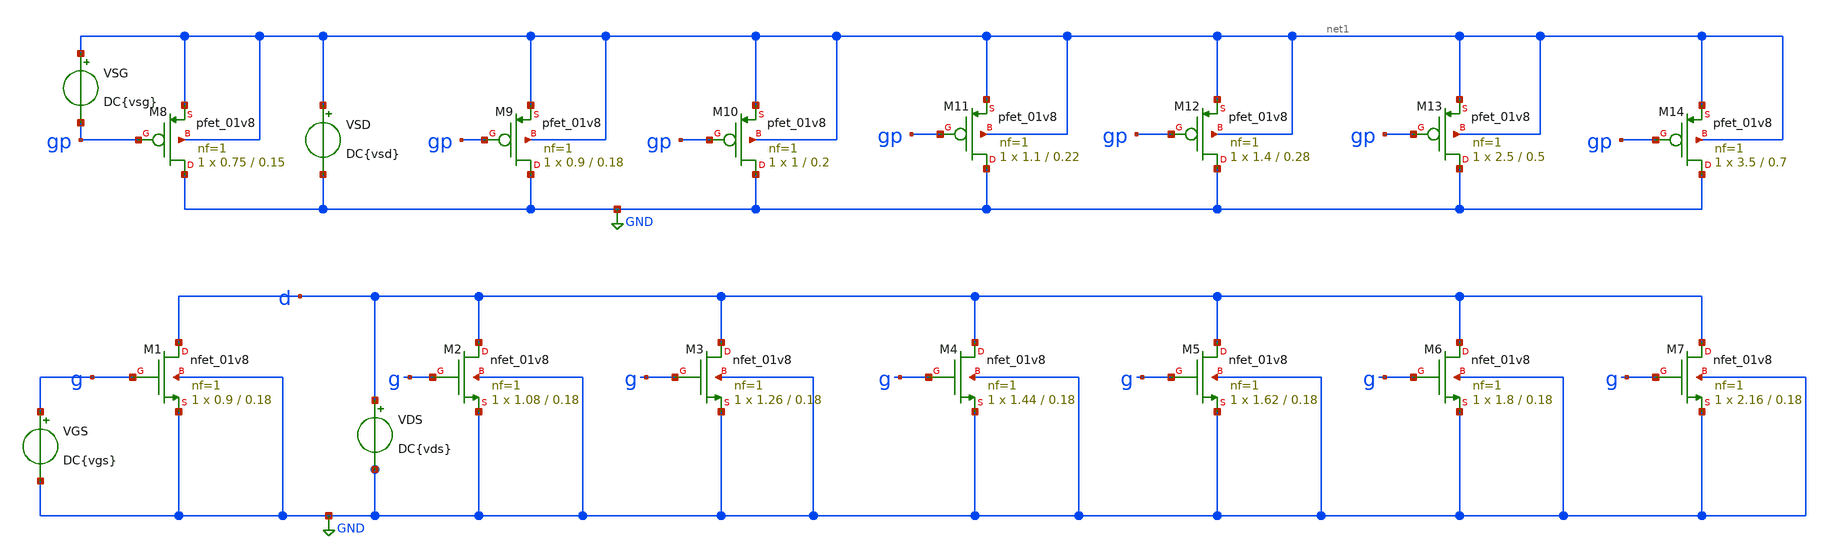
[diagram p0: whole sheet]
** sch_path: XSCHEM/VTH_characterization_01v8.sch
**.subckt VTH_characterization_01v8
XM1 d g GND GND sky130_fd_pr__nfet_01v8 L=0.18 W=0.9 nf=1 ad='int((nf+1)/2) * W/nf * 0.29' as='int((nf+2)/2) * W/nf * 0.29'
+ pd='2*int((nf+1)/2) * (W/nf + 0.29)' ps='2*int((nf+2)/2) * (W/nf + 0.29)' nrd='0.29 / W' nrs='0.29 / W'
+ sa=0 sb=0 sd=0 mult=1 m=1
XM2 d g GND GND sky130_fd_pr__nfet_01v8 L=0.18 W=1.08 nf=1 ad='int((nf+1)/2) * W/nf * 0.29' as='int((nf+2)/2) * W/nf * 0.29'
+ pd='2*int((nf+1)/2) * (W/nf + 0.29)' ps='2*int((nf+2)/2) * (W/nf + 0.29)' nrd='0.29 / W' nrs='0.29 / W'
+ sa=0 sb=0 sd=0 mult=1 m=1
XM3 d g GND GND sky130_fd_pr__nfet_01v8 L=0.18 W=1.26 nf=1 ad='int((nf+1)/2) * W/nf * 0.29' as='int((nf+2)/2) * W/nf * 0.29'
+ pd='2*int((nf+1)/2) * (W/nf + 0.29)' ps='2*int((nf+2)/2) * (W/nf + 0.29)' nrd='0.29 / W' nrs='0.29 / W'
+ sa=0 sb=0 sd=0 mult=1 m=1
VGS g GND DC{vgs}
VDS d GND DC{vds}
XM4 d g GND GND sky130_fd_pr__nfet_01v8 L=0.18 W=1.44 nf=1 ad='int((nf+1)/2) * W/nf * 0.29' as='int((nf+2)/2) * W/nf * 0.29'
+ pd='2*int((nf+1)/2) * (W/nf + 0.29)' ps='2*int((nf+2)/2) * (W/nf + 0.29)' nrd='0.29 / W' nrs='0.29 / W'
+ sa=0 sb=0 sd=0 mult=1 m=1
XM5 d g GND GND sky130_fd_pr__nfet_01v8 L=0.18 W=1.62 nf=1 ad='int((nf+1)/2) * W/nf * 0.29' as='int((nf+2)/2) * W/nf * 0.29'
+ pd='2*int((nf+1)/2) * (W/nf + 0.29)' ps='2*int((nf+2)/2) * (W/nf + 0.29)' nrd='0.29 / W' nrs='0.29 / W'
+ sa=0 sb=0 sd=0 mult=1 m=1
XM6 d g GND GND sky130_fd_pr__nfet_01v8 L=0.18 W=1.8 nf=1 ad='int((nf+1)/2) * W/nf * 0.29' as='int((nf+2)/2) * W/nf * 0.29'
+ pd='2*int((nf+1)/2) * (W/nf + 0.29)' ps='2*int((nf+2)/2) * (W/nf + 0.29)' nrd='0.29 / W' nrs='0.29 / W'
+ sa=0 sb=0 sd=0 mult=1 m=1
XM7 d g GND GND sky130_fd_pr__nfet_01v8 L=0.18 W=2.16 nf=1 ad='int((nf+1)/2) * W/nf * 0.29' as='int((nf+2)/2) * W/nf * 0.29'
+ pd='2*int((nf+1)/2) * (W/nf + 0.29)' ps='2*int((nf+2)/2) * (W/nf + 0.29)' nrd='0.29 / W' nrs='0.29 / W'
+ sa=0 sb=0 sd=0 mult=1 m=1
XM8 GND gp net1 net1 sky130_fd_pr__pfet_01v8 L=0.15 W=0.75 nf=1 ad='int((nf+1)/2) * W/nf * 0.29' as='int((nf+2)/2) * W/nf * 0.29'
+ pd='2*int((nf+1)/2) * (W/nf + 0.29)' ps='2*int((nf+2)/2) * (W/nf + 0.29)' nrd='0.29 / W' nrs='0.29 / W'
+ sa=0 sb=0 sd=0 mult=1 m=1
XM9 GND gp net1 net1 sky130_fd_pr__pfet_01v8 L=0.18 W=0.9 nf=1 ad='int((nf+1)/2) * W/nf * 0.29' as='int((nf+2)/2) * W/nf * 0.29'
+ pd='2*int((nf+1)/2) * (W/nf + 0.29)' ps='2*int((nf+2)/2) * (W/nf + 0.29)' nrd='0.29 / W' nrs='0.29 / W'
+ sa=0 sb=0 sd=0 mult=1 m=1
XM10 GND gp net1 net1 sky130_fd_pr__pfet_01v8 L=0.2 W=1 nf=1 ad='int((nf+1)/2) * W/nf * 0.29' as='int((nf+2)/2) * W/nf * 0.29'
+ pd='2*int((nf+1)/2) * (W/nf + 0.29)' ps='2*int((nf+2)/2) * (W/nf + 0.29)' nrd='0.29 / W' nrs='0.29 / W'
+ sa=0 sb=0 sd=0 mult=1 m=1
XM11 GND gp net1 net1 sky130_fd_pr__pfet_01v8 L=0.22 W=1.1 nf=1 ad='int((nf+1)/2) * W/nf * 0.29' as='int((nf+2)/2) * W/nf * 0.29'
+ pd='2*int((nf+1)/2) * (W/nf + 0.29)' ps='2*int((nf+2)/2) * (W/nf + 0.29)' nrd='0.29 / W' nrs='0.29 / W'
+ sa=0 sb=0 sd=0 mult=1 m=1
XM12 GND gp net1 net1 sky130_fd_pr__pfet_01v8 L=0.28 W=1.4 nf=1 ad='int((nf+1)/2) * W/nf * 0.29' as='int((nf+2)/2) * W/nf * 0.29'
+ pd='2*int((nf+1)/2) * (W/nf + 0.29)' ps='2*int((nf+2)/2) * (W/nf + 0.29)' nrd='0.29 / W' nrs='0.29 / W'
+ sa=0 sb=0 sd=0 mult=1 m=1
XM13 GND gp net1 net1 sky130_fd_pr__pfet_01v8 L=0.5 W=2.5 nf=1 ad='int((nf+1)/2) * W/nf * 0.29' as='int((nf+2)/2) * W/nf * 0.29'
+ pd='2*int((nf+1)/2) * (W/nf + 0.29)' ps='2*int((nf+2)/2) * (W/nf + 0.29)' nrd='0.29 / W' nrs='0.29 / W'
+ sa=0 sb=0 sd=0 mult=1 m=1
XM14 GND gp net1 net1 sky130_fd_pr__pfet_01v8 L=0.7 W=3.5 nf=1 ad='int((nf+1)/2) * W/nf * 0.29' as='int((nf+2)/2) * W/nf * 0.29'
+ pd='2*int((nf+1)/2) * (W/nf + 0.29)' ps='2*int((nf+2)/2) * (W/nf + 0.29)' nrd='0.29 / W' nrs='0.29 / W'
+ sa=0 sb=0 sd=0 mult=1 m=1
VSG net1 gp DC{vsg}
VSD net1 GND DC{vsd}
**** begin user architecture code



* Parameters
.param vds = 1.8
.param vgs = 0.9
.param vsd = 1.8
.param vsg = 0.9
.options TEMPS = 27.0

* Models
.lib /home/karlajcm/skywater130/skywater-pdk/libraries/sky130_fd_pr/latest/models/sky130.lib.spice TT

* Data to save
.save all  @M.XM1.msky130_fd_pr__nfet_01v8[id]  @M.XM1.msky130_fd_pr__nfet_01v8[gm]  @M.XM1.msky130_fd_pr__nfet_01v8[vth]  @M.XM1.msky130_fd_pr__nfet_01v8[vds]  @M.XM1.msky130_fd_pr__nfet_01v8[vdsat]  @M.XM1.msky130_fd_pr__nfet_01v8[vgs]  @M.XM1.msky130_fd_pr__nfet_01v8[cgg]  @M.XM2.msky130_fd_pr__nfet_01v8[id]  @M.XM2.msky130_fd_pr__nfet_01v8[gm]  @M.XM2.msky130_fd_pr__nfet_01v8[vth]  @M.XM2.msky130_fd_pr__nfet_01v8[vds]  @M.XM2.msky130_fd_pr__nfet_01v8[vdsat]  @M.XM2.msky130_fd_pr__nfet_01v8[vgs]  @M.XM2.msky130_fd_pr__nfet_01v8[cgg]  @M.XM3.msky130_fd_pr__nfet_01v8[id]  @M.XM3.msky130_fd_pr__nfet_01v8[gm]  @M.XM3.msky130_fd_pr__nfet_01v8[vth]  @M.XM3.msky130_fd_pr__nfet_01v8[vds]  @M.XM3.msky130_fd_pr__nfet_01v8[vdsat]  @M.XM3.msky130_fd_pr__nfet_01v8[vgs]  @M.XM3.msky130_fd_pr__nfet_01v8[cgg]  @M.XM4.msky130_fd_pr__nfet_01v8[id]  @M.XM4.msky130_fd_pr__nfet_01v8[gm]  @M.XM4.msky130_fd_pr__nfet_01v8[vth]  @M.XM4.msky130_fd_pr__nfet_01v8[vds]  @M.XM4.msky130_fd_pr__nfet_01v8[vdsat]  @M.XM4.msky130_fd_pr__nfet_01v8[vgs]  @M.XM4.msky130_fd_pr__nfet_01v8[cgg]  @M.XM5.msky130_fd_pr__nfet_01v8[id]  @M.XM5.msky130_fd_pr__nfet_01v8[gm]  @M.XM5.msky130_fd_pr__nfet_01v8[vth]  @M.XM5.msky130_fd_pr__nfet_01v8[vds]  @M.XM5.msky130_fd_pr__nfet_01v8[vdsat]  @M.XM5.msky130_fd_pr__nfet_01v8[vgs]  @M.XM5.msky130_fd_pr__nfet_01v8[cgg]  @M.XM6.msky130_fd_pr__nfet_01v8[id]  @M.XM6.msky130_fd_pr__nfet_01v8[gm]  @M.XM6.msky130_fd_pr__nfet_01v8[vth]  @M.XM6.msky130_fd_pr__nfet_01v8[vds]  @M.XM6.msky130_fd_pr__nfet_01v8[vdsat]  @M.XM6.msky130_fd_pr__nfet_01v8[vgs]  @M.XM6.msky130_fd_pr__nfet_01v8[cgg]  @M.XM7.msky130_fd_pr__nfet_01v8[id]  @M.XM7.msky130_fd_pr__nfet_01v8[gm]  @M.XM7.msky130_fd_pr__nfet_01v8[vth]  @M.XM7.msky130_fd_pr__nfet_01v8[vds]  @M.XM7.msky130_fd_pr__nfet_01v8[vdsat]  @M.XM7.msky130_fd_pr__nfet_01v8[vgs]  @M.XM7.msky130_fd_pr__nfet_01v8[cgg]  @M.XM8.msky130_fd_pr__pfet_01v8[id]  @M.XM8.msky130_fd_pr__pfet_01v8[gm]  @M.XM8.msky130_fd_pr__pfet_01v8[vth]  @M.XM8.msky130_fd_pr__pfet_01v8[vds]  @M.XM8.msky130_fd_pr__pfet_01v8[vdsat]  @M.XM8.msky130_fd_pr__pfet_01v8[vgs]  @M.XM8.msky130_fd_pr__pfet_01v8[cgg]  @M.XM9.msky130_fd_pr__pfet_01v8[id]  @M.XM9.msky130_fd_pr__pfet_01v8[gm]  @M.XM9.msky130_fd_pr__pfet_01v8[vth]  @M.XM9.msky130_fd_pr__pfet_01v8[vds]  @M.XM9.msky130_fd_pr__pfet_01v8[vdsat]  @M.XM9.msky130_fd_pr__pfet_01v8[vgs]  @M.XM9.msky130_fd_pr__pfet_01v8[cgg]  @M.XM10.msky130_fd_pr__pfet_01v8[id]  @M.XM10.msky130_fd_pr__pfet_01v8[gm]  @M.XM10.msky130_fd_pr__pfet_01v8[vth]  @M.XM10.msky130_fd_pr__pfet_01v8[vds]  @M.XM10.msky130_fd_pr__pfet_01v8[vdsat]  @M.XM10.msky130_fd_pr__pfet_01v8[vgs]  @M.XM10.msky130_fd_pr__pfet_01v8[cgg]  @M.XM11.msky130_fd_pr__pfet_01v8[id]  @M.XM11.msky130_fd_pr__pfet_01v8[gm]  @M.XM11.msky130_fd_pr__pfet_01v8[vth]  @M.XM11.msky130_fd_pr__pfet_01v8[vds]  @M.XM11.msky130_fd_pr__pfet_01v8[vdsat]  @M.XM11.msky130_fd_pr__pfet_01v8[vgs]  @M.XM11.msky130_fd_pr__pfet_01v8[cgg]  @M.XM12.msky130_fd_pr__pfet_01v8[id]  @M.XM12.msky130_fd_pr__pfet_01v8[gm]  @M.XM12.msky130_fd_pr__pfet_01v8[vth]  @M.XM12.msky130_fd_pr__pfet_01v8[vds]  @M.XM12.msky130_fd_pr__pfet_01v8[vdsat]  @M.XM12.msky130_fd_pr__pfet_01v8[vgs]  @M.XM12.msky130_fd_pr__pfet_01v8[cgg]  @M.XM13.msky130_fd_pr__pfet_01v8[id]  @M.XM13.msky130_fd_pr__pfet_01v8[gm]  @M.XM13.msky130_fd_pr__pfet_01v8[vth]  @M.XM13.msky130_fd_pr__pfet_01v8[vds]  @M.XM13.msky130_fd_pr__pfet_01v8[vdsat]  @M.XM13.msky130_fd_pr__pfet_01v8[vgs]  @M.XM13.msky130_fd_pr__pfet_01v8[cgg]  @M.XM14.msky130_fd_pr__pfet_01v8[id]  @M.XM14.msky130_fd_pr__pfet_01v8[gm]  @M.XM14.msky130_fd_pr__pfet_01v8[vth]  @M.XM14.msky130_fd_pr__pfet_01v8[vds]  @M.XM14.msky130_fd_pr__pfet_01v8[vdsat]  @M.XM14.msky130_fd_pr__pfet_01v8[vgs]  @M.XM14.msky130_fd_pr__pfet_01v8[cgg]

* Simulation
.control
  dc VDS 0 1.8 0.01 VGS 0 1.8 0.3 VSD 0 1.8 0.01 VSG 0 1.8 0.3
  setplot dc1
  plot @M.XM1.msky130_fd_pr__nfet_01v8[id] @M.XM2.msky130_fd_pr__nfet_01v8[id] @M.XM3.msky130_fd_pr__nfet_01v8[id]
+ @M.XM4.msky130_fd_pr__nfet_01v8[id] @M.XM5.msky130_fd_pr__nfet_01v8[id] @M.XM6.msky130_fd_pr__nfet_01v8[id]
+ @M.XM7.msky130_fd_pr__nfet_01v8[id] ylabel Id xlabel Vds title 'NMOS: Id vs Vds vs Vgs'
  plot @M.XM8.msky130_fd_pr__pfet_01v8[id] @M.XM9.msky130_fd_pr__pfet_01v8[id] @M.XM10.msky130_fd_pr__pfet_01v8[id]
+ @M.XM11.msky130_fd_pr__pfet_01v8[id] @M.XM12.msky130_fd_pr__pfet_01v8[id] @M.XM13.msky130_fd_pr__pfet_01v8[id]
+ @M.XM14.msky130_fd_pr__pfet_01v8[id] ylabel Id xlabel Vsd title 'PMOS:Id vs Vsd vs Vsg'
  set filetype = ascii
  write VTH_characterization_01v8_dc1.raw

  alterparam vds = 0
  alterparam vsd = 0
  reset
  dc VGS -1.8 1.8 0.01 VSG -1.8 1.8 0.01
  setplot dc2
  plot @M.XM1.msky130_fd_pr__nfet_01v8[cgg] @M.XM2.msky130_fd_pr__nfet_01v8[cgg] @M.XM3.msky130_fd_pr__nfet_01v8[cgg]
+ @M.XM4.msky130_fd_pr__nfet_01v8[cgg] @M.XM5.msky130_fd_pr__nfet_01v8[cgg] @M.XM6.msky130_fd_pr__nfet_01v8[cgg]
+ @M.XM7.msky130_fd_pr__nfet_01v8[cgg] ylabel Cgg xlabel Vgs title 'NMOS:Cgg vs Vgs'
  plot @M.XM8.msky130_fd_pr__pfet_01v8[cgg] @M.XM9.msky130_fd_pr__pfet_01v8[cgg] @M.XM10.msky130_fd_pr__pfet_01v8[cgg]
+ @M.XM11.msky130_fd_pr__pfet_01v8[cgg] @M.XM12.msky130_fd_pr__pfet_01v8[cgg] @M.XM13.msky130_fd_pr__pfet_01v8[cgg]
+ @M.XM14.msky130_fd_pr__pfet_01v8[cgg] ylabel Cgg xlabel Vgs title 'PMOS:Cgg vs Vsg'
  set filetype = ascii
  write VTH_characterization_01v8_dc2.raw

  reset
  dc VGS -1.8 1.8 0.01 VSG -1.8 1.8 0.01
  setplot dc3
  plot @M.XM1.msky130_fd_pr__nfet_01v8[vth] @M.XM2.msky130_fd_pr__nfet_01v8[vth] @M.XM3.msky130_fd_pr__nfet_01v8[vth]
+ @M.XM4.msky130_fd_pr__nfet_01v8[vth] @M.XM5.msky130_fd_pr__nfet_01v8[vth] @M.XM6.msky130_fd_pr__nfet_01v8[vth]
+ @M.XM7.msky130_fd_pr__nfet_01v8[vth] ylabel Vth xlabel Vgs title 'NMOS:Vth vs Vgs'
  plot @M.XM8.msky130_fd_pr__pfet_01v8[vth] @M.XM9.msky130_fd_pr__pfet_01v8[vth] @M.XM10.msky130_fd_pr__pfet_01v8[vth]
+ @M.XM11.msky130_fd_pr__pfet_01v8[vth] @M.XM12.msky130_fd_pr__pfet_01v8[vth] @M.XM13.msky130_fd_pr__pfet_01v8[vth]
+ @M.XM14.msky130_fd_pr__pfet_01v8[vth] ylabel Vth xlabel Vsg title 'PMOS:Vth vs Vsg'
  set filetype = ascii
  write VTH_characterization_01v8_dc3.raw

  reset
  unset filetype
  op
  save all
  write VTH_characterization_01v8.raw

.endc

.end


**** end user architecture code
**.ends
.GLOBAL GND
.end
